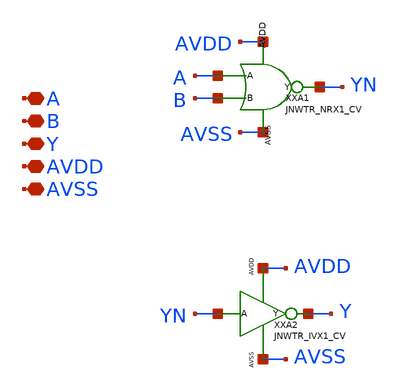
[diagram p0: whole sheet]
** sch_path: design/JNW_TR_SKY130A/JNWTR_ORX2_CV.sch
**.subckt JNWTR_ORX2_CV A B Y AVDD AVSS
*.iopin A
*.iopin B
*.iopin Y
*.iopin AVDD
*.iopin AVSS
XXA1 A B YN AVDD AVSS JNWTR_NRX1_CV
XXA2 YN Y AVDD AVSS JNWTR_IVX1_CV
**.ends
.end
